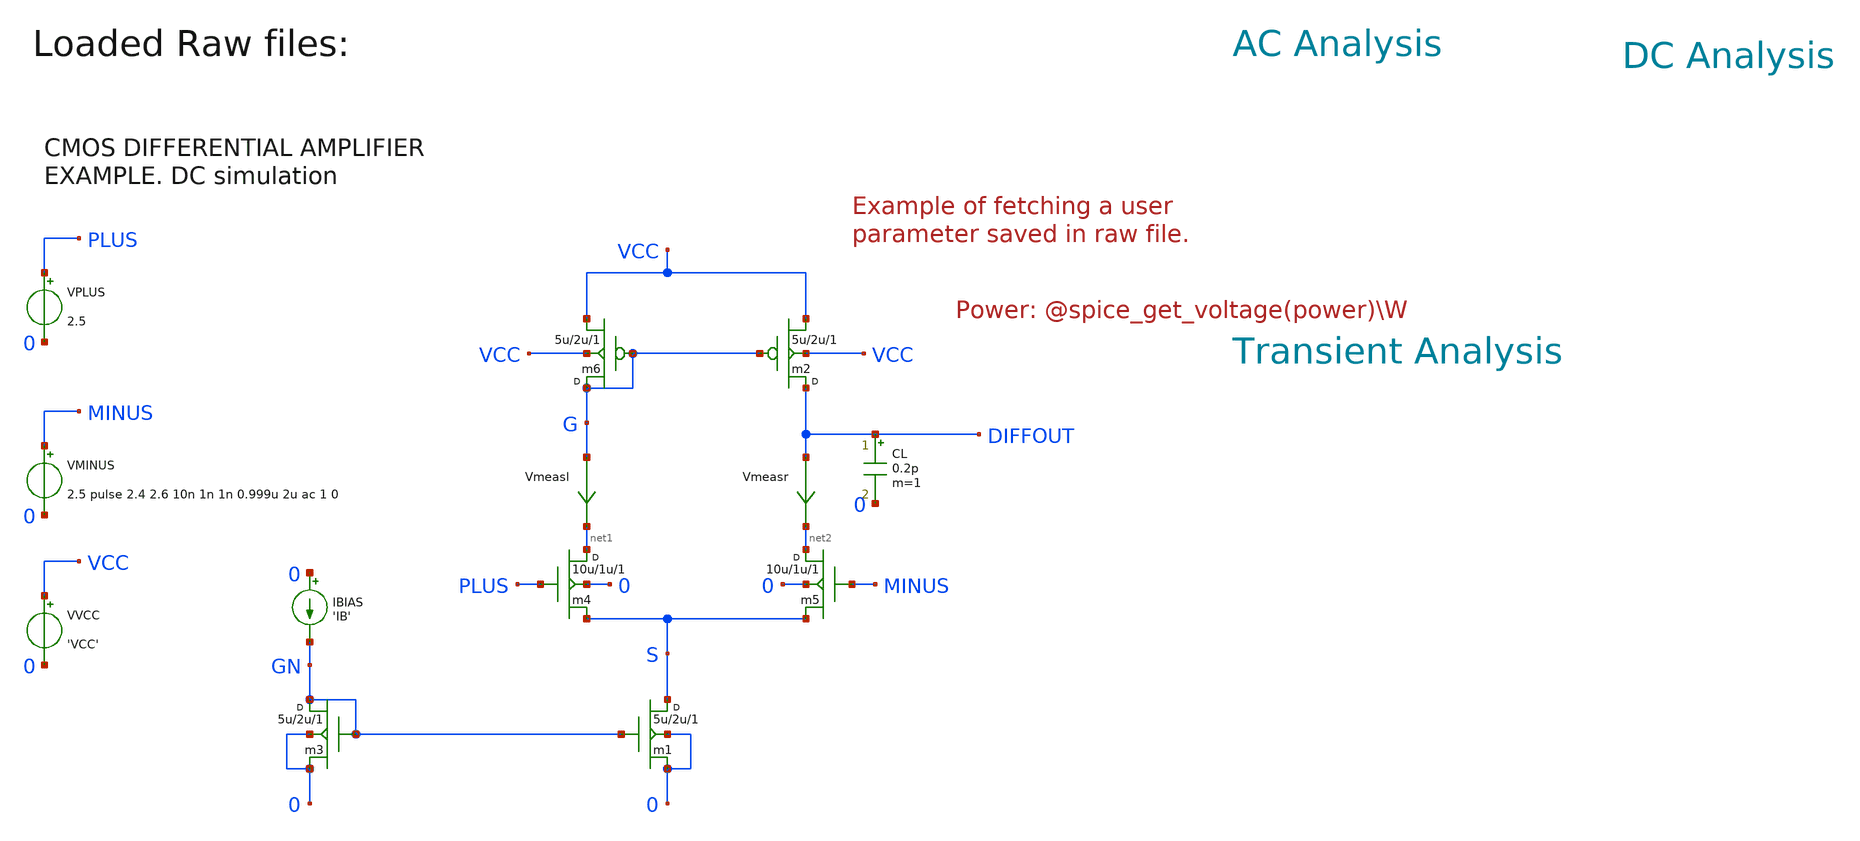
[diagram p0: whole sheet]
** sch_path: examples/xschem_examples/cmos_example.sch
* Copyright (C) 1998-2023 Stefan Frederik Schippers
* This program is free software; you can redistribute it and/or modify
* it under the terms of the GNU General Public License as published by
* the Free Software Foundation; either version 2 of the License, or
* (at your option) any later version.
* This program is distributed in the hope that it will be useful,
* but WITHOUT ANY WARRANTY; without even the implied warranty of
* MERCHANTABILITY or FITNESS FOR A PARTICULAR PURPOSE.  See the
* GNU General Public License for more details.
* You should have received a copy of the GNU General Public License
* along with this program; if not, write to the Free Software
**.subckt cmos_example
m1 S GN 0 0 cmosn w=5u l=2u m=1
m2 DIFFOUT G VCC VCC cmosp w=5u l=2u m=1
VVCC VCC 0 'VCC'
m3 GN GN 0 0 cmosn w=5u l=2u m=1
IBIAS 0 GN 'IB'
m4 net1 PLUS S 0 cmosn w=10u l=1u m=1
m5 net2 MINUS S 0 cmosn w=10u l=1u m=1
m6 G G VCC VCC cmosp w=5u l=2u m=1
VMINUS MINUS 0 2.5 pulse 2.4 2.6 10n 1n 1n 0.999u 2u ac 1 0
VPLUS PLUS 0 2.5
CL DIFFOUT 0 0.2p m=1
Vmeasr DIFFOUT net2 0
.save i(vmeasr)
Vmeasl G net1 0
.save i(vmeasl)
**** begin user architecture code


.temp 30
.param IB=2u
.param VCC = 5
** models are generally not free: you must download
** SPICE models for active devices and put them into the below
** referenced file in netlist/simulation directory.
** http://bwrcs.eecs.berkeley.edu/Classes/icdesign/ee241_s00/ASSIGNMENTS/TSMC035-n96g-params.txt
.include "models_cmos_example.txt"
.option savecurrents
.save all @m4[gm] @m5[gm] @m1[gm]
.control
  save all alli
  op
  let power=-v(vcc) * i(vvcc)
  settype power power
  write cmos_example_ngspice.raw
  set appendwrite
  dc vminus 2.3 2.7 0.001
  write cmos_example_ngspice.raw
  tran 0.5n 5u
  write cmos_example_ngspice.raw
  ac dec 10 1 1G
  remzerovec
  write cmos_example_ngspice.raw

  alterparam IB=10u
  reset
  save all
  dc vminus 2.4 2.6 0.001
  write cmos_example_ngspice.raw
  tran 0.5n 5u
  write cmos_example_ngspice.raw
  ac dec 10 1 1G
  remzerovec
  write cmos_example_ngspice.raw

  alterparam IB=100u
  reset
  save all
  dc vminus 2.3 2.7 0.001
  write cmos_example_ngspice.raw
  tran 0.5n 5u
  write cmos_example_ngspice.raw
  ac dec 10 1 1G
  remzerovec
  write cmos_example_ngspice.raw
  quit 0
.endc







**** end user architecture code
**.ends
.end
